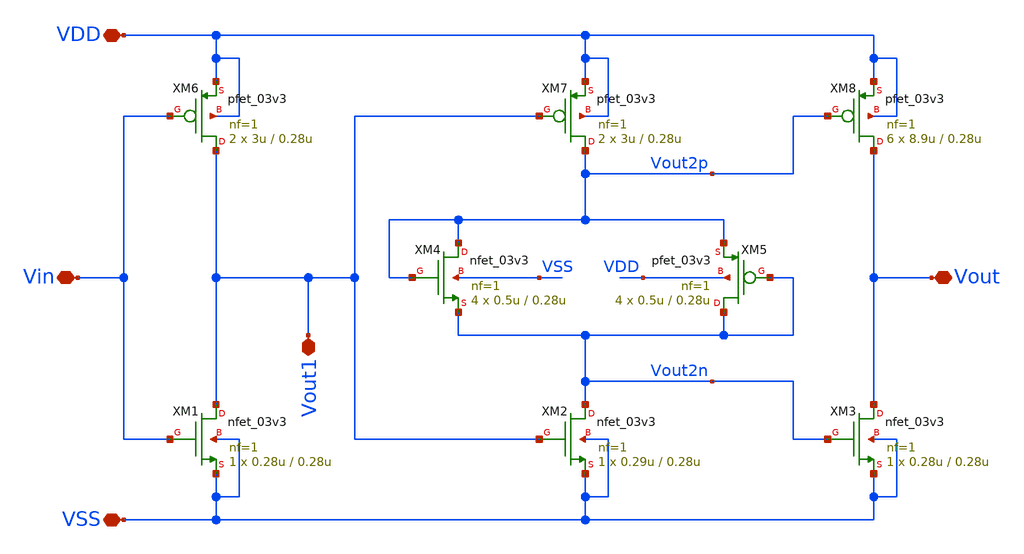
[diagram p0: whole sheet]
** sch_path: designs/DS_modulator/ring_amp/xschem/ring_amp.sch
**.subckt ring_amp VDD VSS Vin Vout Vout1
*.iopin VDD
*.iopin VSS
*.iopin Vin
*.iopin Vout
*.iopin Vout1
XM1 Vout1 Vin VSS VSS nfet_03v3 L=0.28u W=0.28u nf=1 ad='int((nf+1)/2) * W/nf * 0.18u' as='int((nf+2)/2) * W/nf * 0.18u'
+ pd='2*int((nf+1)/2) * (W/nf + 0.18u)' ps='2*int((nf+2)/2) * (W/nf + 0.18u)' nrd='0.18u / W' nrs='0.18u / W'
+ sa=0 sb=0 sd=0 m=1
XM4 Vout2p Vout2p Vout2n VSS nfet_03v3 L=0.28u W=0.5u nf=1 ad='int((nf+1)/2) * W/nf * 0.18u' as='int((nf+2)/2) * W/nf * 0.18u'
+ pd='2*int((nf+1)/2) * (W/nf + 0.18u)' ps='2*int((nf+2)/2) * (W/nf + 0.18u)' nrd='0.18u / W' nrs='0.18u / W'
+ sa=0 sb=0 sd=0 m=4
XM2 Vout2n Vout1 VSS VSS nfet_03v3 L=0.28u W=0.29u nf=1 ad='int((nf+1)/2) * W/nf * 0.18u' as='int((nf+2)/2) * W/nf * 0.18u'
+ pd='2*int((nf+1)/2) * (W/nf + 0.18u)' ps='2*int((nf+2)/2) * (W/nf + 0.18u)' nrd='0.18u / W' nrs='0.18u / W'
+ sa=0 sb=0 sd=0 m=1
XM3 Vout Vout2n VSS VSS nfet_03v3 L=0.28u W=0.28u nf=1 ad='int((nf+1)/2) * W/nf * 0.18u' as='int((nf+2)/2) * W/nf * 0.18u'
+ pd='2*int((nf+1)/2) * (W/nf + 0.18u)' ps='2*int((nf+2)/2) * (W/nf + 0.18u)' nrd='0.18u / W' nrs='0.18u / W'
+ sa=0 sb=0 sd=0 m=1
XM5 Vout2n Vout2n Vout2p VDD pfet_03v3 L=0.28u W=0.5u nf=1 ad='int((nf+1)/2) * W/nf * 0.18u' as='int((nf+2)/2) * W/nf * 0.18u'
+ pd='2*int((nf+1)/2) * (W/nf + 0.18u)' ps='2*int((nf+2)/2) * (W/nf + 0.18u)' nrd='0.18u / W' nrs='0.18u / W'
+ sa=0 sb=0 sd=0 m=4
XM6 Vout1 Vin VDD VDD pfet_03v3 L=0.28u W=3u nf=1 ad='int((nf+1)/2) * W/nf * 0.18u' as='int((nf+2)/2) * W/nf * 0.18u'
+ pd='2*int((nf+1)/2) * (W/nf + 0.18u)' ps='2*int((nf+2)/2) * (W/nf + 0.18u)' nrd='0.18u / W' nrs='0.18u / W'
+ sa=0 sb=0 sd=0 m=2
XM7 Vout2p Vout1 VDD VDD pfet_03v3 L=0.28u W=3u nf=1 ad='int((nf+1)/2) * W/nf * 0.18u' as='int((nf+2)/2) * W/nf * 0.18u'
+ pd='2*int((nf+1)/2) * (W/nf + 0.18u)' ps='2*int((nf+2)/2) * (W/nf + 0.18u)' nrd='0.18u / W' nrs='0.18u / W'
+ sa=0 sb=0 sd=0 m=2
XM8 Vout Vout2p VDD VDD pfet_03v3 L=0.28u W=8.9u nf=1 ad='int((nf+1)/2) * W/nf * 0.18u' as='int((nf+2)/2) * W/nf * 0.18u'
+ pd='2*int((nf+1)/2) * (W/nf + 0.18u)' ps='2*int((nf+2)/2) * (W/nf + 0.18u)' nrd='0.18u / W' nrs='0.18u / W'
+ sa=0 sb=0 sd=0 m=6
**.ends
.end
